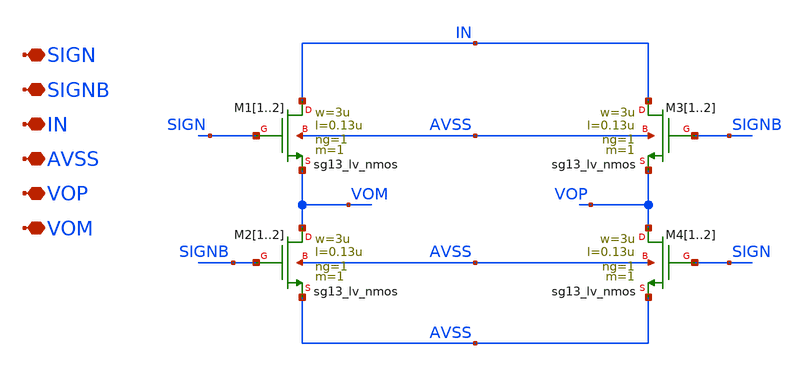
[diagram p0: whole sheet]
** sch_path: current_generator/analog/DAC/schematics/dsw.sch
**.subckt dsw SIGN SIGNB IN AVSS VOP VOM
*.iopin SIGN
*.iopin SIGNB
*.iopin IN
*.iopin AVSS
*.iopin VOP
*.iopin VOM
XM11 IN SIGN VOM AVSS sg13_lv_nmos w=3u l=0.13u ng=1 m=1 mm_ok=1
XM12 IN SIGN VOM AVSS sg13_lv_nmos w=3u l=0.13u ng=1 m=1 mm_ok=1
XM21 VOM SIGNB AVSS AVSS sg13_lv_nmos w=3u l=0.13u ng=1 m=1 mm_ok=1
XM22 VOM SIGNB AVSS AVSS sg13_lv_nmos w=3u l=0.13u ng=1 m=1 mm_ok=1
XM31 IN SIGNB VOP AVSS sg13_lv_nmos w=3u l=0.13u ng=1 m=1 mm_ok=1
XM32 IN SIGNB VOP AVSS sg13_lv_nmos w=3u l=0.13u ng=1 m=1 mm_ok=1
XM41 VOP SIGN AVSS AVSS sg13_lv_nmos w=3u l=0.13u ng=1 m=1 mm_ok=1
XM42 VOP SIGN AVSS AVSS sg13_lv_nmos w=3u l=0.13u ng=1 m=1 mm_ok=1
**.ends
.end
